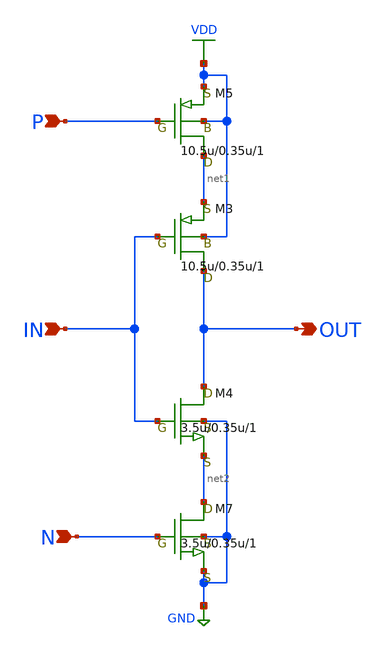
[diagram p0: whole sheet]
** sch_path: LR_hokari/LR_Work2/symbol/CLOCKEDINVERTER.sch
**.subckt CLOCKEDINVERTER OUT IN P N
*.opin OUT
*.ipin IN
*.ipin P
*.ipin N
M3 OUT IN net1 VDD pch w=10.5u l=0.35u as=0 ps=0 ad=0 pd=0 m=1
M4 OUT IN net2 GND nch w=3.5u l=0.35u as=0 ps=0 ad=0 pd=0 m=1
M5 net1 P VDD VDD pch w=10.5u l=0.35u as=0 ps=0 ad=0 pd=0 m=1
M7 net2 N GND GND nch w=3.5u l=0.35u as=0 ps=0 ad=0 pd=0 m=1
**.ends
.GLOBAL VDD
.GLOBAL GND
.end
